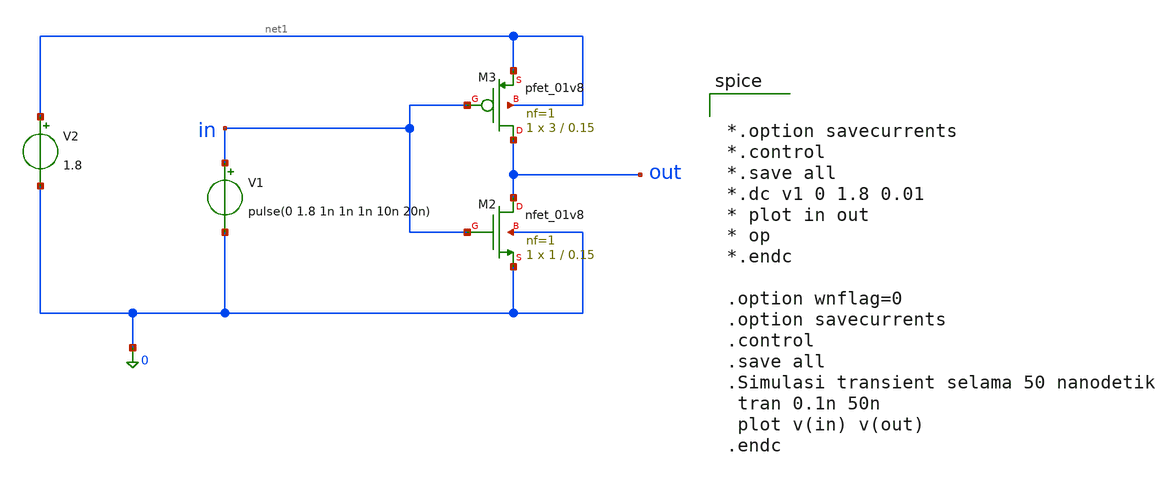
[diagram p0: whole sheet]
** sch_path: sch/Inverter_CMOS.sch
**.subckt Inverter_CMOS
XM2 out in 0 0 sky130_fd_pr__nfet_01v8 L=0.15 W=1 nf=1 ad='int((1 + 1)/2) * 1 / 1 * 0.29' as='int((1 + 2)/2) * 1 / 1 * 0.29'
+ pd='2*int((1 + 1)/2) * (1 / 1 + 0.29)' ps='2*int((1 + 2)/2) * (1 / 1 + 0.29)' nrd='0.29 / 1 ' nrs='0.29 / 1 '
+ sa=0 sb=0 sd=0 mult=1 m=1
XM3 out in net1 net1 sky130_fd_pr__pfet_01v8 L=0.15 W=3 nf=1 ad='int((1 + 1)/2) * 3 / 1 * 0.29' as='int((1 + 2)/2) * 3 / 1 * 0.29'
+ pd='2*int((1 + 1)/2) * (3 / 1 + 0.29)' ps='2*int((1 + 2)/2) * (3 / 1 + 0.29)' nrd='0.29 / 3 ' nrs='0.29 / 3 '
+ sa=0 sb=0 sd=0 mult=1 m=1
V1 in 0 pulse(0 1.8 1n 1n 1n 10n 20n)
V2 net1 0 1.8
**** begin user architecture code
 .lib /foss/pdks/ciel/sky130/versions/7b70722e33c03fcb5dabcf4d479fb0822d9251c9/sky130A/libs.tech/ngspice/sky130.lib.spice tt


*.option savecurrents
*.control
*.save all
*.dc v1 0 1.8 0.01
* plot in out
* op
*.endc

.option wnflag=0
.option savecurrents
.control
.save all
.Simulasi transient selama 50 nanodetik
 tran 0.1n 50n
 plot v(in) v(out)
.endc


**** end user architecture code
**.ends
.end
